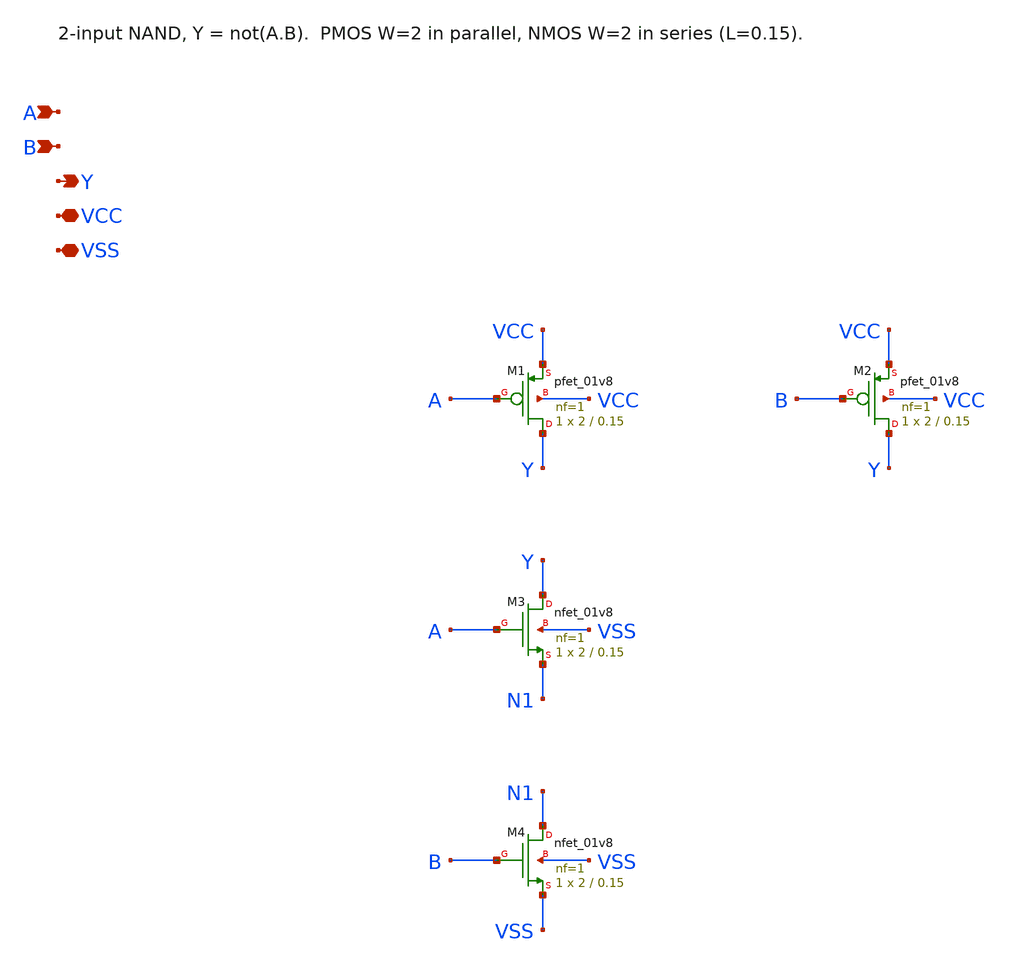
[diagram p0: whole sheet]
** sch_path: nand2.sch
**.subckt nand2 A B Y VCC VSS
*.ipin A
*.ipin B
*.opin Y
*.iopin VCC
*.iopin VSS
XM1 Y A VCC VCC sky130_fd_pr__pfet_01v8 L=0.15 W=2 nf=1 ad='int((nf+1)/2) * W/nf * 0.29' as='int((nf+2)/2) * W/nf * 0.29'
+ pd='2*int((nf+1)/2) * (W/nf + 0.29)' ps='2*int((nf+2)/2) * (W/nf + 0.29)' nrd='0.29 / W' nrs='0.29 / W'
+ sa=0 sb=0 sd=0 mult=1 m=1
XM2 Y B VCC VCC sky130_fd_pr__pfet_01v8 L=0.15 W=2 nf=1 ad='int((nf+1)/2) * W/nf * 0.29' as='int((nf+2)/2) * W/nf * 0.29'
+ pd='2*int((nf+1)/2) * (W/nf + 0.29)' ps='2*int((nf+2)/2) * (W/nf + 0.29)' nrd='0.29 / W' nrs='0.29 / W'
+ sa=0 sb=0 sd=0 mult=1 m=1
XM3 Y A N1 VSS sky130_fd_pr__nfet_01v8 L=0.15 W=2 nf=1 ad='int((nf+1)/2) * W/nf * 0.29' as='int((nf+2)/2) * W/nf * 0.29'
+ pd='2*int((nf+1)/2) * (W/nf + 0.29)' ps='2*int((nf+2)/2) * (W/nf + 0.29)' nrd='0.29 / W' nrs='0.29 / W'
+ sa=0 sb=0 sd=0 mult=1 m=1
XM4 N1 B VSS VSS sky130_fd_pr__nfet_01v8 L=0.15 W=2 nf=1 ad='int((nf+1)/2) * W/nf * 0.29' as='int((nf+2)/2) * W/nf * 0.29'
+ pd='2*int((nf+1)/2) * (W/nf + 0.29)' ps='2*int((nf+2)/2) * (W/nf + 0.29)' nrd='0.29 / W' nrs='0.29 / W'
+ sa=0 sb=0 sd=0 mult=1 m=1
**.ends
.end
